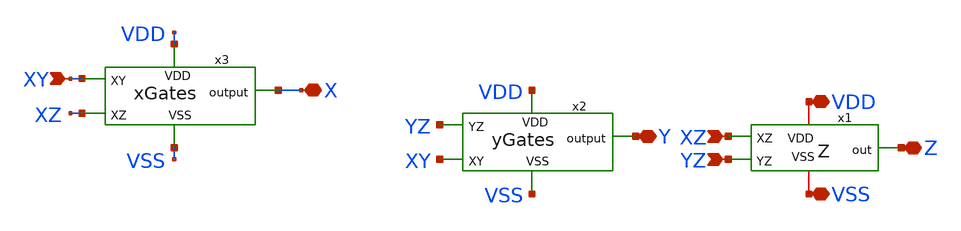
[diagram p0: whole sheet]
** sch_path: FINAL/XSCHEM/DECODER/DECODER.sch
**.subckt DECODER XY XZ VDD VSS X YZ Y Z
*.ipin XY
*.ipin XZ
*.iopin VDD
*.iopin VSS
*.iopin X
*.ipin YZ
*.iopin Y
*.iopin Z
x2 YZ XY VDD Y VSS yGates
x1 VSS VDD XZ YZ Z Z
x3 VDD XY X XZ VSS xGates
**.ends
.end
